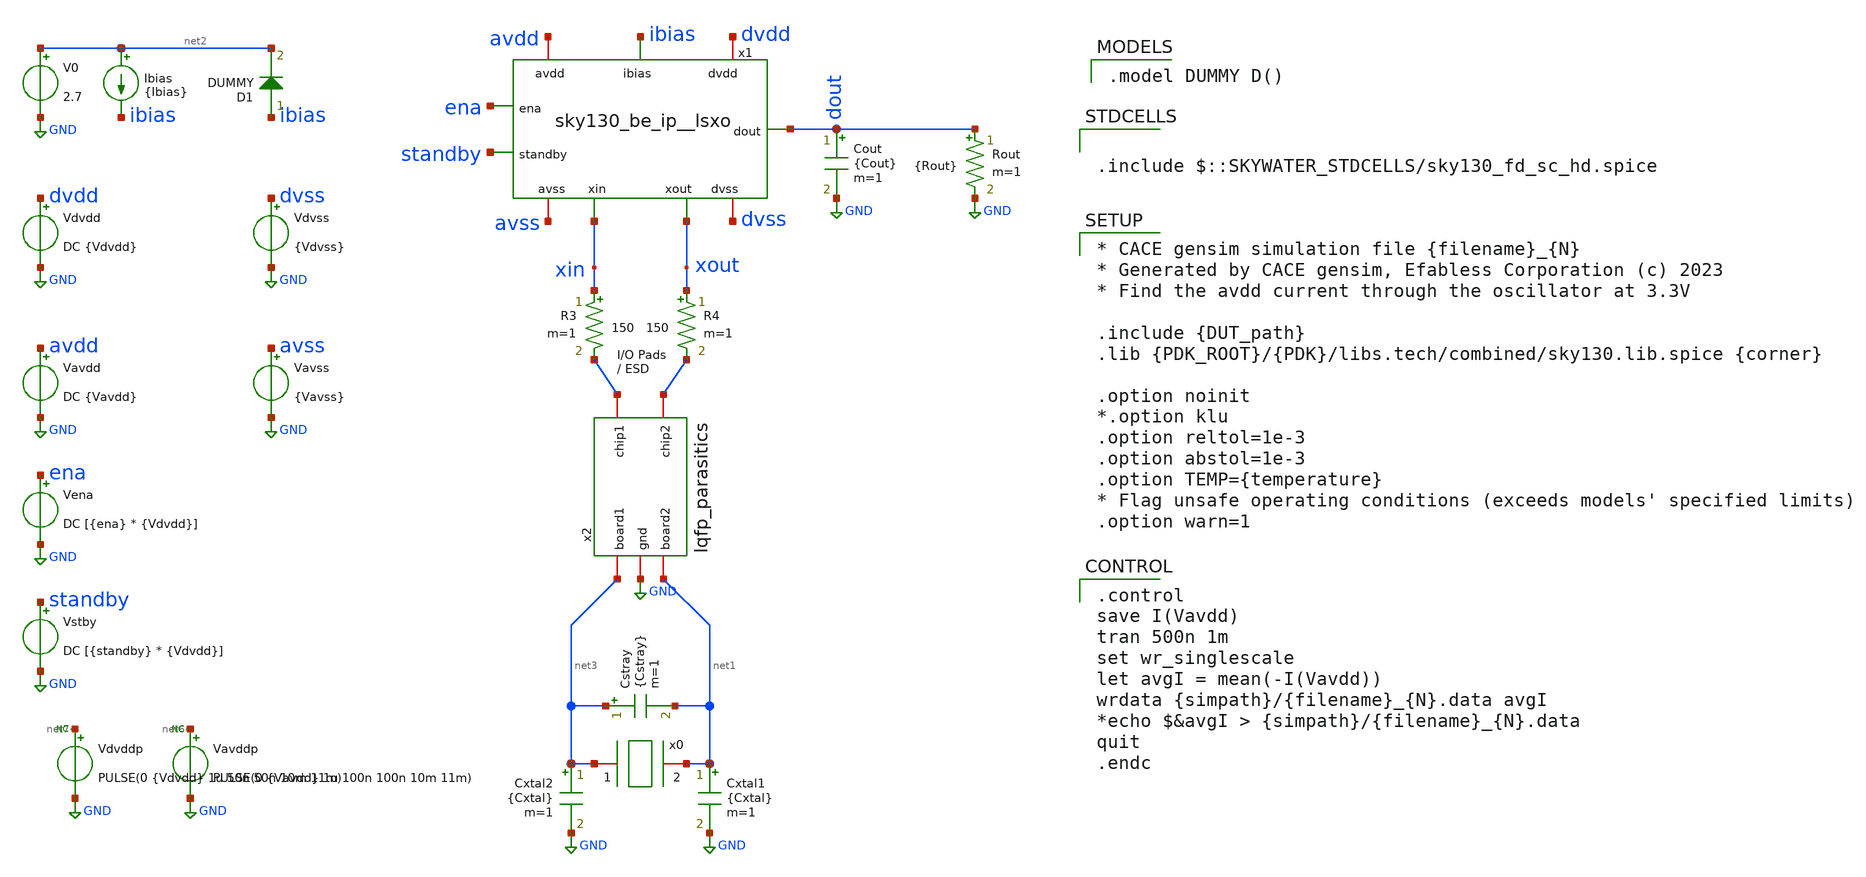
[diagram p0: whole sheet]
** sch_path: cace/templates/tb_current_avdd.sch

.include $::SKYWATER_STDCELLS/sky130_fd_sc_hd.spice

**.subckt tb_current_avdd
Cxtal2 net3 GND {Cxtal} m=1
Cxtal1 net1 GND {Cxtal} m=1
Cstray net3 net1 {Cstray} m=1
Ibias net2 ibias {Ibias}
Cout dout GND {Cout} m=1
V0 net2 GND 2.7
Vstby standby GND DC [{standby} * {Vdvdd}]
R3 xin net4 150 m=1
R4 xout net5 150 m=1
x2 net5 net4 GND net3 net1 lqfp_parasitics
Vena ena GND DC [{ena} * {Vdvdd}]
D1 ibias net2 DUMMY area=100
x1 avdd avss dvdd dvss ibias ena standby dout xin xout sky130_be_ip__lsxo
Vdvss dvss GND {Vdvss}
Vavss avss GND {Vavss}
Rout dout GND {Rout} m=1
x0 net3 net1 xtal_iqd_125_1
Vavddp net6 GND PULSE(0 {Vavdd} 1u 100n 100n 10m 11m)
Vdvddp net7 GND PULSE(0 {Vdvdd} 1u 50n 50n 10m 11m)
Vavdd avdd GND DC {Vavdd}
Vdvdd dvdd GND DC {Vdvdd}
* noconn #net7
* noconn #net6
**** begin user architecture code

.model DUMMY D()


.control
save I(Vavdd)
tran 500n 1m
set wr_singlescale
let avgI = mean(-I(Vavdd))
wrdata {simpath}/{filename}_{N}.data avgI
*echo $&avgI > {simpath}/{filename}_{N}.data
quit
.endc



* CACE gensim simulation file {filename}_{N}
* Generated by CACE gensim, Efabless Corporation (c) 2023
* Find the avdd current through the oscillator at 3.3V

.include {DUT_path}
.lib {PDK_ROOT}/{PDK}/libs.tech/combined/sky130.lib.spice {corner}

.option noinit
*.option klu
.option reltol=1e-3
.option abstol=1e-3
.option TEMP={temperature}
* Flag unsafe operating conditions (exceeds models' specified limits)
.option warn=1


**** end user architecture code
**.ends
.GLOBAL GND
.end
